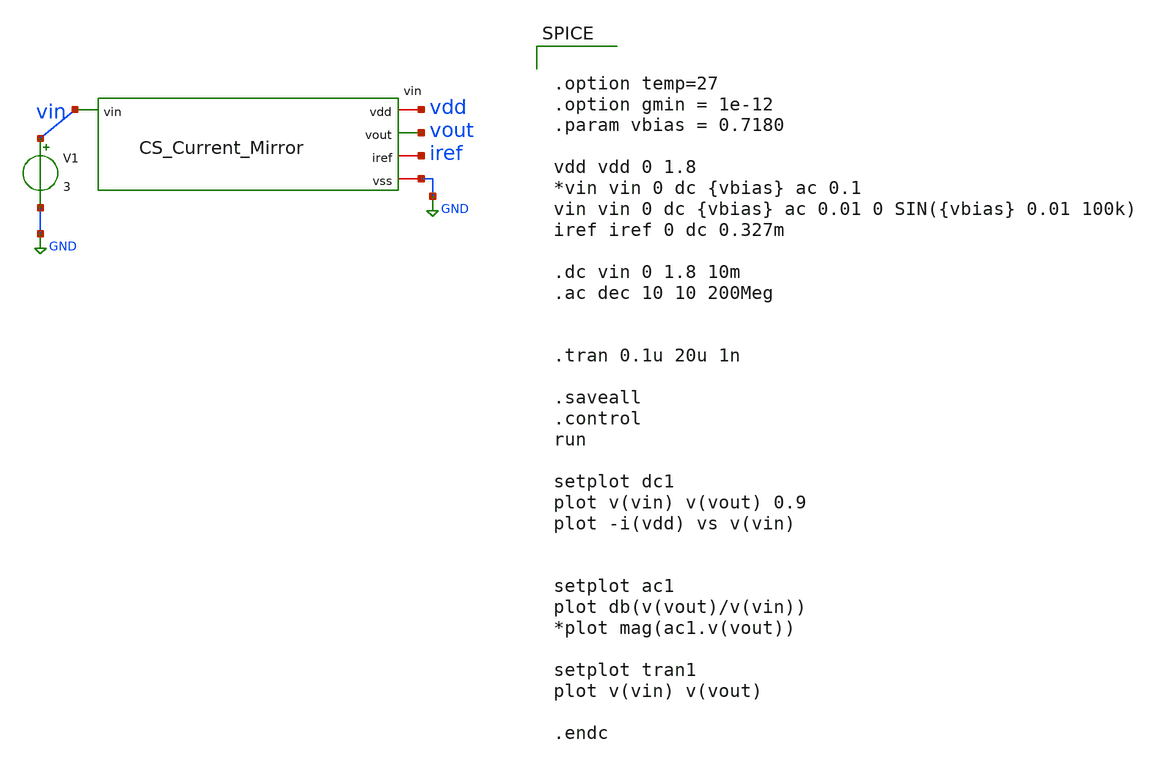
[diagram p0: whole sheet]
** sch_path: tb/tb_CS_Current_Mirror.sch
**.subckt tb_CS_Current_Mirror
vin vdd vout iref vin GND CS_Current_Mirror
V1 vin GND 3
**** begin user architecture code

** opencircuitdesign pdks install
.lib $::SKYWATER_MODELS/sky130.lib.spice tt




.option temp=27
.option gmin = 1e-12
.param vbias = 0.7180

vdd vdd 0 1.8
*vin vin 0 dc {vbias} ac 0.1
vin vin 0 dc {vbias} ac 0.01 0 SIN({vbias} 0.01 100k)
iref iref 0 dc 0.327m

.dc vin 0 1.8 10m
.ac dec 10 10 200Meg


.tran 0.1u 20u 1n

.saveall
.control
run

setplot dc1
plot v(vin) v(vout) 0.9
plot -i(vdd) vs v(vin)


setplot ac1
plot db(v(vout)/v(vin))
*plot mag(ac1.v(vout))

setplot tran1
plot v(vin) v(vout)

.endc


**** end user architecture code
**.ends

* expanding   symbol:  /foss/designs/Assignment2/src/CS_Current_Mirror.sym # of pins=5
** sym_path: src/CS_Current_Mirror.sym
** sch_path: src/CS_Current_Mirror.sch
.subckt CS_Current_Mirror vdd vout iref vin vss
*.ipin vin
*.opin vout
*.iopin vdd
*.iopin iref
*.iopin vss
**** begin user architecture code


.option temp=27
.option gmin = 1e-12
.param vbias = 0.7180

vss vss 0 0
vdd vdd 0 1.8
*vin vin 0 dc {vbias} ac 0.1
vin vin 0 dc {vbias} ac 0.01 0 SIN({vbias} 0.01 100k)
iref iref 0 dc 0.327m

.dc vin 0 1.8 10m
.ac dec 10 10 200Meg


.tran 0.1u 20u 1n

.saveall
.control
run

setplot dc1
plot v(vin) v(vout) 0.9
plot -i(vdd) vs v(vin)


setplot ac1
plot db(v(vout)/v(vin))
*plot mag(ac1.v(vout))

setplot tran1
plot v(vin) v(vout)

.endc


**** end user architecture code
XC1 vout vss sky130_fd_pr__cap_mim_m3_1 W=40 L=87 MF=1 m=1
XM2 vout iref vdd vdd sky130_fd_pr__pfet_01v8 L=1 W=170 nf=15 ad='int((nf+1)/2) * W/nf * 0.29' as='int((nf+2)/2) * W/nf * 0.29'
+ pd='2*int((nf+1)/2) * (W/nf + 0.29)' ps='2*int((nf+2)/2) * (W/nf + 0.29)' nrd='0.29 / W' nrs='0.29 / W'
+ sa=0 sb=0 sd=0 mult=1 m=1
XM1 vout vin vss vss sky130_fd_pr__nfet_01v8 L=1 W=120 nf=12 ad='int((nf+1)/2) * W/nf * 0.29' as='int((nf+2)/2) * W/nf * 0.29'
+ pd='2*int((nf+1)/2) * (W/nf + 0.29)' ps='2*int((nf+2)/2) * (W/nf + 0.29)' nrd='0.29 / W' nrs='0.29 / W'
+ sa=0 sb=0 sd=0 mult=1 m=1
XM3 iref iref vdd vdd sky130_fd_pr__pfet_01v8 L=1 W=170 nf=15 ad='int((nf+1)/2) * W/nf * 0.29' as='int((nf+2)/2) * W/nf * 0.29'
+ pd='2*int((nf+1)/2) * (W/nf + 0.29)' ps='2*int((nf+2)/2) * (W/nf + 0.29)' nrd='0.29 / W' nrs='0.29 / W'
+ sa=0 sb=0 sd=0 mult=1 m=1
.ends

.GLOBAL GND
.end
